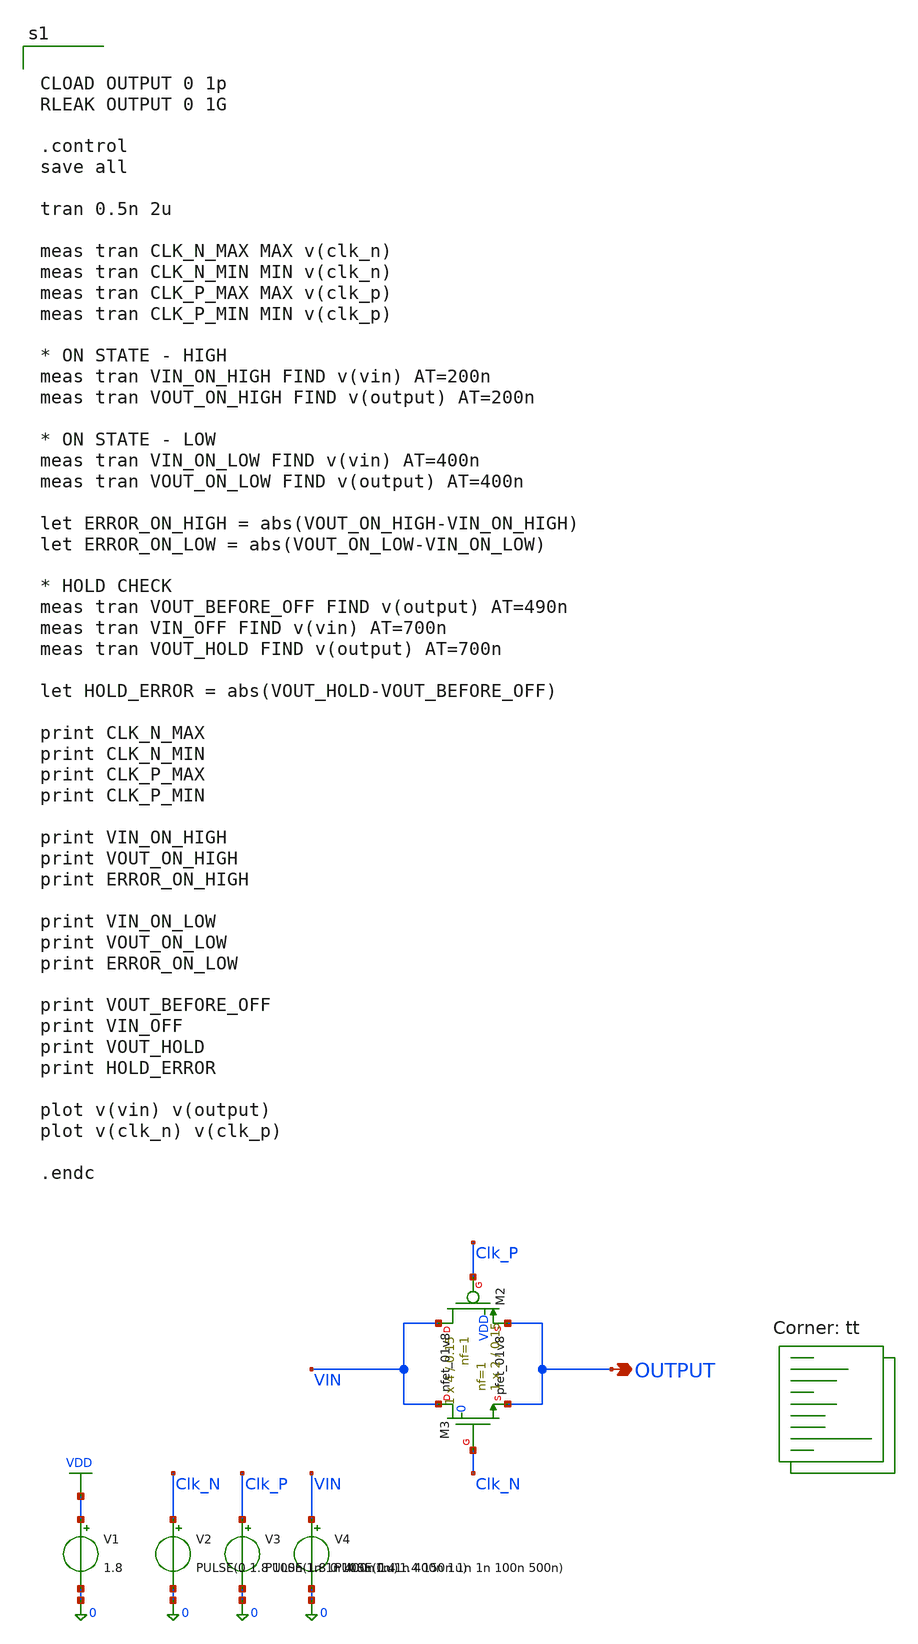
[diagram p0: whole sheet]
** sch_path: blocks/02_CMFB/xschem/Test_TG.sch
**.subckt Test_TG OUTPUT
*.opin OUTPUT
XM2 VIN Clk_P OUTPUT VDD sky130_fd_pr__pfet_01v8 L=0.15 W=4 nf=1 ad='int((1 + 1)/2) * 4 / 1 * 0.29' as='int((1 + 2)/2) * 4 / 1 * 0.29'
+ pd='2*int((1 + 1)/2) * (4 / 1 + 0.29)' ps='2*int((1 + 2)/2) * (4 / 1 + 0.29)' nrd='0.29 / 4 ' nrs='0.29 / 4 '
+ sa=0 sb=0 sd=0 mult=1 m=1
XM3 VIN Clk_N OUTPUT 0 sky130_fd_pr__nfet_01v8 L=0.15 W=2 nf=1 ad='int((1 + 1)/2) * 2 / 1 * 0.29' as='int((1 + 2)/2) * 2 / 1 * 0.29'
+ pd='2*int((1 + 1)/2) * (2 / 1 + 0.29)' ps='2*int((1 + 2)/2) * (2 / 1 + 0.29)' nrd='0.29 / 2 ' nrs='0.29 / 2 '
+ sa=0 sb=0 sd=0 mult=1 m=1
V1 VDD 0 1.8
V2 Clk_N 0 PULSE(0 1.8 100n 1n 1n 400n 1u)
V3 Clk_P 0 PULSE(1.8 0 100n 1n 1n 400n 1u)
V4 VIN 0 PULSE(0.4 1.4 150n 1n 1n 100n 500n)
**** begin user architecture code


CLOAD OUTPUT 0 1p
RLEAK OUTPUT 0 1G

.control
save all

tran 0.5n 2u

meas tran CLK_N_MAX MAX v(clk_n)
meas tran CLK_N_MIN MIN v(clk_n)
meas tran CLK_P_MAX MAX v(clk_p)
meas tran CLK_P_MIN MIN v(clk_p)

* ON STATE - HIGH
meas tran VIN_ON_HIGH FIND v(vin) AT=200n
meas tran VOUT_ON_HIGH FIND v(output) AT=200n

* ON STATE - LOW
meas tran VIN_ON_LOW FIND v(vin) AT=400n
meas tran VOUT_ON_LOW FIND v(output) AT=400n

let ERROR_ON_HIGH = abs(VOUT_ON_HIGH-VIN_ON_HIGH)
let ERROR_ON_LOW = abs(VOUT_ON_LOW-VIN_ON_LOW)

* HOLD CHECK
meas tran VOUT_BEFORE_OFF FIND v(output) AT=490n
meas tran VIN_OFF FIND v(vin) AT=700n
meas tran VOUT_HOLD FIND v(output) AT=700n

let HOLD_ERROR = abs(VOUT_HOLD-VOUT_BEFORE_OFF)

print CLK_N_MAX
print CLK_N_MIN
print CLK_P_MAX
print CLK_P_MIN

print VIN_ON_HIGH
print VOUT_ON_HIGH
print ERROR_ON_HIGH

print VIN_ON_LOW
print VOUT_ON_LOW
print ERROR_ON_LOW

print VOUT_BEFORE_OFF
print VIN_OFF
print VOUT_HOLD
print HOLD_ERROR

plot v(vin) v(output)
plot v(clk_n) v(clk_p)

.endc


.lib $::SKYWATER_MODELS/sky130.lib.spice tt
**** end user architecture code
**.ends
.GLOBAL VDD
.end
